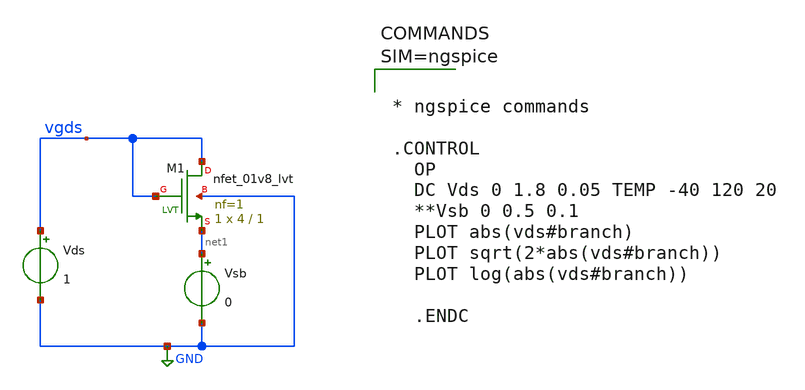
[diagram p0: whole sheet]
** sch_path: xschem/nfet1.sch
**.subckt nfet1
XM1 vgds vgds net1 GND sky130_fd_pr__nfet_01v8_lvt L=1 W=4 nf=1 ad='int((1 + 1)/2) * 4 / 1 * 0.29' as='int((1 + 2)/2) * 4 / 1 * 0.29'
+ pd='2*int((1 + 1)/2) * (4 / 1 + 0.29)' ps='2*int((1 + 2)/2) * (4 / 1 + 0.29)' nrd='0.29 / 4 ' nrs='0.29 / 4 '
+ sa=0 sb=0 sd=0 mult=1 m=1
Vds vgds GND 1
Vsb net1 GND 0
**** begin user architecture code

** opencircuitdesign pdks install
.lib $::SKYWATER_MODELS/sky130.lib.spice tt




* ngspice commands

.CONTROL
  OP
  DC Vds 0 1.8 0.05 TEMP -40 120 20
  **Vsb 0 0.5 0.1
  PLOT abs(vds#branch)
  PLOT sqrt(2*abs(vds#branch))
  PLOT log(abs(vds#branch))

  .ENDC



**** end user architecture code
**.ends
.GLOBAL GND
.end
